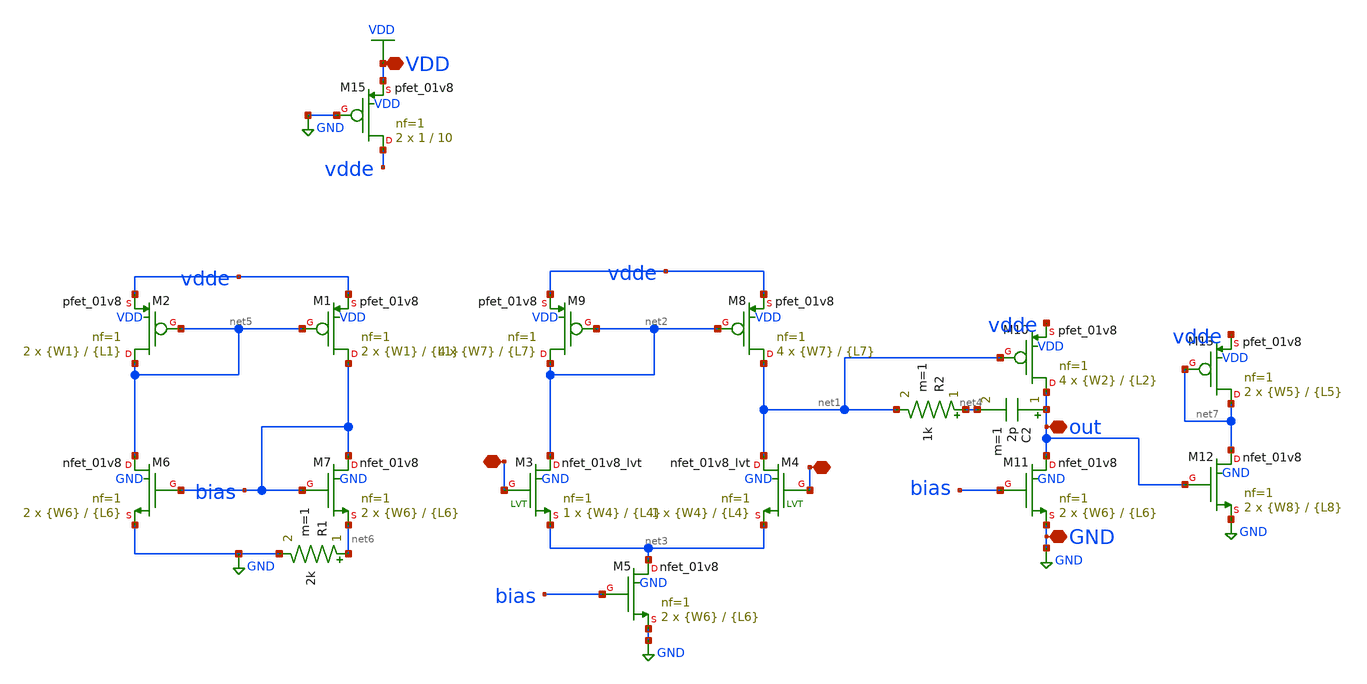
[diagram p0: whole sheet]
** sch_path: xschem/op5.1.sch
**.subckt op5.1 GND - + VDD out
*.iopin GND
*.iopin -
*.iopin +
*.iopin VDD
*.iopin out
C2 out net4 2p m=1
R2 net4 net1 1k m=1
XM8 net1 net2 vdde VDD sky130_fd_pr__pfet_01v8 L={L7} W={W7} nf=1 ad='int((nf+1)/2) * W/nf * 0.29' as='int((nf+2)/2) * W/nf * 0.29'
+ pd='2*int((nf+1)/2) * (W/nf + 0.29)' ps='2*int((nf+2)/2) * (W/nf + 0.29)' nrd='0.29 / W' nrs='0.29 / W'
+ sa=0 sb=0 sd=0 mult=4 m=4
XM9 net2 net2 vdde VDD sky130_fd_pr__pfet_01v8 L={L7} W={W7} nf=1 ad='int((nf+1)/2) * W/nf * 0.29' as='int((nf+2)/2) * W/nf * 0.29'
+ pd='2*int((nf+1)/2) * (W/nf + 0.29)' ps='2*int((nf+2)/2) * (W/nf + 0.29)' nrd='0.29 / W' nrs='0.29 / W'
+ sa=0 sb=0 sd=0 mult=4 m=4
XM5 net3 bias GND GND sky130_fd_pr__nfet_01v8 L={L6} W={W6} nf=1 ad='int((nf+1)/2) * W/nf * 0.29' as='int((nf+2)/2) * W/nf * 0.29'
+ pd='2*int((nf+1)/2) * (W/nf + 0.29)' ps='2*int((nf+2)/2) * (W/nf + 0.29)' nrd='0.29 / W' nrs='0.29 / W'
+ sa=0 sb=0 sd=0 mult=2 m=2
XM10 out net1 vdde VDD sky130_fd_pr__pfet_01v8 L={L2} W={W2} nf=1 ad='int((nf+1)/2) * W/nf * 0.29' as='int((nf+2)/2) * W/nf * 0.29'
+ pd='2*int((nf+1)/2) * (W/nf + 0.29)' ps='2*int((nf+2)/2) * (W/nf + 0.29)' nrd='0.29 / W' nrs='0.29 / W'
+ sa=0 sb=0 sd=0 mult=4 m=4
XM1 bias net5 vdde VDD sky130_fd_pr__pfet_01v8 L={L1} W={W1} nf=1 ad='int((nf+1)/2) * W/nf * 0.29' as='int((nf+2)/2) * W/nf * 0.29'
+ pd='2*int((nf+1)/2) * (W/nf + 0.29)' ps='2*int((nf+2)/2) * (W/nf + 0.29)' nrd='0.29 / W' nrs='0.29 / W'
+ sa=0 sb=0 sd=0 mult=2 m=2
XM2 net5 net5 vdde VDD sky130_fd_pr__pfet_01v8 L={L1} W={W1} nf=1 ad='int((nf+1)/2) * W/nf * 0.29' as='int((nf+2)/2) * W/nf * 0.29'
+ pd='2*int((nf+1)/2) * (W/nf + 0.29)' ps='2*int((nf+2)/2) * (W/nf + 0.29)' nrd='0.29 / W' nrs='0.29 / W'
+ sa=0 sb=0 sd=0 mult=2 m=2
XM6 net5 bias GND GND sky130_fd_pr__nfet_01v8 L={L6} W={W6} nf=1 ad='int((nf+1)/2) * W/nf * 0.29' as='int((nf+2)/2) * W/nf * 0.29'
+ pd='2*int((nf+1)/2) * (W/nf + 0.29)' ps='2*int((nf+2)/2) * (W/nf + 0.29)' nrd='0.29 / W' nrs='0.29 / W'
+ sa=0 sb=0 sd=0 mult=2 m=2
XM7 bias bias net6 GND sky130_fd_pr__nfet_01v8 L={L6} W={W6} nf=1 ad='int((nf+1)/2) * W/nf * 0.29' as='int((nf+2)/2) * W/nf * 0.29'
+ pd='2*int((nf+1)/2) * (W/nf + 0.29)' ps='2*int((nf+2)/2) * (W/nf + 0.29)' nrd='0.29 / W' nrs='0.29 / W'
+ sa=0 sb=0 sd=0 mult=2 m=2
R1 net6 GND 2k m=1
XM3 net2 - net3 GND sky130_fd_pr__nfet_01v8_lvt L={L4} W={W4} nf=1 ad='int((nf+1)/2) * W/nf * 0.29' as='int((nf+2)/2) * W/nf * 0.29'
+ pd='2*int((nf+1)/2) * (W/nf + 0.29)' ps='2*int((nf+2)/2) * (W/nf + 0.29)' nrd='0.29 / W' nrs='0.29 / W'
+ sa=0 sb=0 sd=0 mult=1 m=1
XM4 net1 + net3 GND sky130_fd_pr__nfet_01v8_lvt L={L4} W={W4} nf=1 ad='int((nf+1)/2) * W/nf * 0.29' as='int((nf+2)/2) * W/nf * 0.29'
+ pd='2*int((nf+1)/2) * (W/nf + 0.29)' ps='2*int((nf+2)/2) * (W/nf + 0.29)' nrd='0.29 / W' nrs='0.29 / W'
+ sa=0 sb=0 sd=0 mult=1 m=1
XM11 out bias GND GND sky130_fd_pr__nfet_01v8 L={L6} W={W6} nf=1 ad='int((nf+1)/2) * W/nf * 0.29' as='int((nf+2)/2) * W/nf * 0.29'
+ pd='2*int((nf+1)/2) * (W/nf + 0.29)' ps='2*int((nf+2)/2) * (W/nf + 0.29)' nrd='0.29 / W' nrs='0.29 / W'
+ sa=0 sb=0 sd=0 mult=2 m=2
XM12 net7 out GND GND sky130_fd_pr__nfet_01v8 L={L8} W={W8} nf=1 ad='int((nf+1)/2) * W/nf * 0.29' as='int((nf+2)/2) * W/nf * 0.29'
+ pd='2*int((nf+1)/2) * (W/nf + 0.29)' ps='2*int((nf+2)/2) * (W/nf + 0.29)' nrd='0.29 / W' nrs='0.29 / W'
+ sa=0 sb=0 sd=0 mult=2 m=2
XM13 net7 net7 vdde VDD sky130_fd_pr__pfet_01v8 L={L5} W={W5} nf=1 ad='int((nf+1)/2) * W/nf * 0.29' as='int((nf+2)/2) * W/nf * 0.29'
+ pd='2*int((nf+1)/2) * (W/nf + 0.29)' ps='2*int((nf+2)/2) * (W/nf + 0.29)' nrd='0.29 / W' nrs='0.29 / W'
+ sa=0 sb=0 sd=0 mult=2 m=2
XM15 vdde GND VDD VDD sky130_fd_pr__pfet_01v8 L=10 W=1 nf=1 ad='int((nf+1)/2) * W/nf * 0.29' as='int((nf+2)/2) * W/nf * 0.29'
+ pd='2*int((nf+1)/2) * (W/nf + 0.29)' ps='2*int((nf+2)/2) * (W/nf + 0.29)' nrd='0.29 / W' nrs='0.29 / W'
+ sa=0 sb=0 sd=0 mult=2 m=2
**** begin user architecture code


**************
*PMOS cms
.param L1=20
.param W1=0.5

**************
*PMOS current differential
.param L7=10
.param W7=1

**************
*differential Pair
.param L4=10
.param W4=1

**************
*NMOS current control
.param L6=10
.param W6=1

**************
*Second Stage
.param L2=5
.param W2=1

**************
*NMOS current second stage
.param L3=10
.param W3=1

**************
*Current source Stage
.param L5=20
.param W5=1

**************
*Third Stage
.param L8=20
.param W8=1


**** end user architecture code
**.ends
.GLOBAL GND
.GLOBAL VDD
.end
